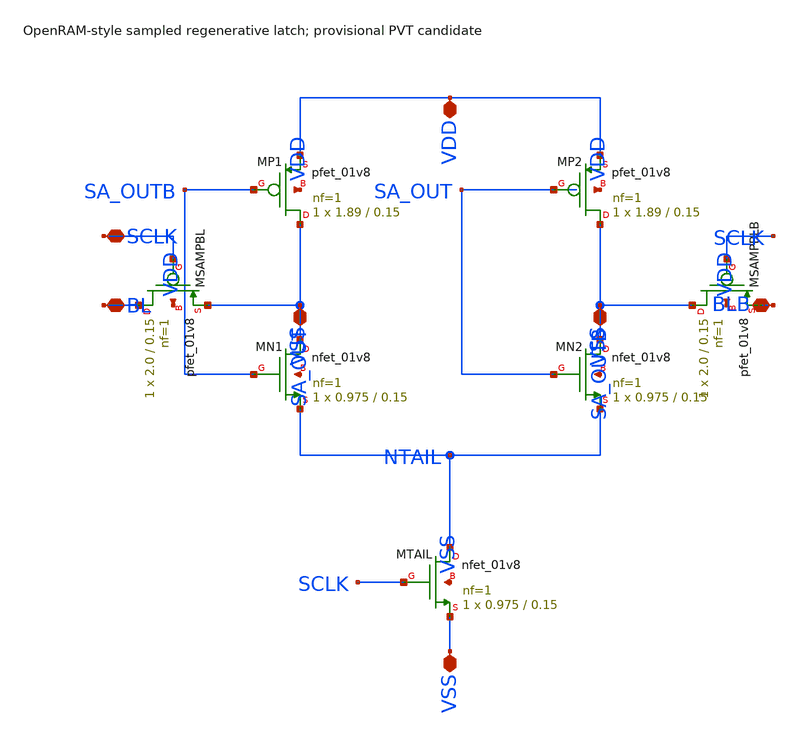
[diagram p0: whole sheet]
** sch_path: release/phase1/cells/sense_amp/sense_amp.sch
**.subckt sense_amp VDD VSS BL BLB SCLK SA_OUT SA_OUTB
*.iopin VDD
*.iopin VSS
*.iopin BL
*.iopin BLB
*.iopin SCLK
*.iopin SA_OUT
*.iopin SA_OUTB
XMP1 SA_OUT SA_OUTB VDD VDD sky130_fd_pr__pfet_01v8 L=0.15 W=1.89 nf=1 ad='int((nf+1)/2) * W/nf * 0.29'
+ as='int((nf+2)/2) * W/nf * 0.29' pd='2*int((nf+1)/2) * (W/nf + 0.29)' ps='2*int((nf+2)/2) * (W/nf + 0.29)'
+ nrd='0.29 / W' nrs='0.29 / W' sa=0 sb=0 sd=0 mult=1 m=1
XMN1 SA_OUT SA_OUTB NTAIL VSS sky130_fd_pr__nfet_01v8 L=0.15 W=0.975 nf=1 ad='int((1 + 1)/2) * 0.975 / 1 * 0.29'
+ as='int((1 + 2)/2) * 0.975 / 1 * 0.29' pd='2*int((1 + 1)/2) * (0.975 / 1 + 0.29)' ps='2*int((1 + 2)/2) * (0.975 / 1 + 0.29)'
+ nrd='0.29 / 0.975 ' nrs='0.29 / 0.975 ' sa=0 sb=0 sd=0 mult=1 m=1
XMP2 SA_OUTB SA_OUT VDD VDD sky130_fd_pr__pfet_01v8 L=0.15 W=1.89 nf=1 ad='int((nf+1)/2) * W/nf * 0.29'
+ as='int((nf+2)/2) * W/nf * 0.29' pd='2*int((nf+1)/2) * (W/nf + 0.29)' ps='2*int((nf+2)/2) * (W/nf + 0.29)'
+ nrd='0.29 / W' nrs='0.29 / W' sa=0 sb=0 sd=0 mult=1 m=1
XMN2 SA_OUTB SA_OUT NTAIL VSS sky130_fd_pr__nfet_01v8 L=0.15 W=0.975 nf=1 ad='int((1 + 1)/2) * 0.975 / 1 * 0.29'
+ as='int((1 + 2)/2) * 0.975 / 1 * 0.29' pd='2*int((1 + 1)/2) * (0.975 / 1 + 0.29)' ps='2*int((1 + 2)/2) * (0.975 / 1 + 0.29)'
+ nrd='0.29 / 0.975 ' nrs='0.29 / 0.975 ' sa=0 sb=0 sd=0 mult=1 m=1
XMSAMPBL BL SCLK SA_OUT VDD sky130_fd_pr__pfet_01v8 L=0.15 W=2.0 nf=1 ad='int((nf+1)/2) * W/nf * 0.29'
+ as='int((nf+2)/2) * W/nf * 0.29' pd='2*int((nf+1)/2) * (W/nf + 0.29)' ps='2*int((nf+2)/2) * (W/nf + 0.29)'
+ nrd='0.29 / W' nrs='0.29 / W' sa=0 sb=0 sd=0 mult=1 m=1
XMSAMPBLB SA_OUTB SCLK BLB VDD sky130_fd_pr__pfet_01v8 L=0.15 W=2.0 nf=1 ad='int((nf+1)/2) * W/nf * 0.29'
+ as='int((nf+2)/2) * W/nf * 0.29' pd='2*int((nf+1)/2) * (W/nf + 0.29)' ps='2*int((nf+2)/2) * (W/nf + 0.29)'
+ nrd='0.29 / W' nrs='0.29 / W' sa=0 sb=0 sd=0 mult=1 m=1
XMTAIL NTAIL SCLK VSS VSS sky130_fd_pr__nfet_01v8 L=0.15 W=0.975 nf=1 ad='int((1 + 1)/2) * 0.975 / 1 * 0.29'
+ as='int((1 + 2)/2) * 0.975 / 1 * 0.29' pd='2*int((1 + 1)/2) * (0.975 / 1 + 0.29)' ps='2*int((1 + 2)/2) * (0.975 / 1 + 0.29)'
+ nrd='0.29 / 0.975 ' nrs='0.29 / 0.975 ' sa=0 sb=0 sd=0 mult=1 m=1
**.ends
.end
